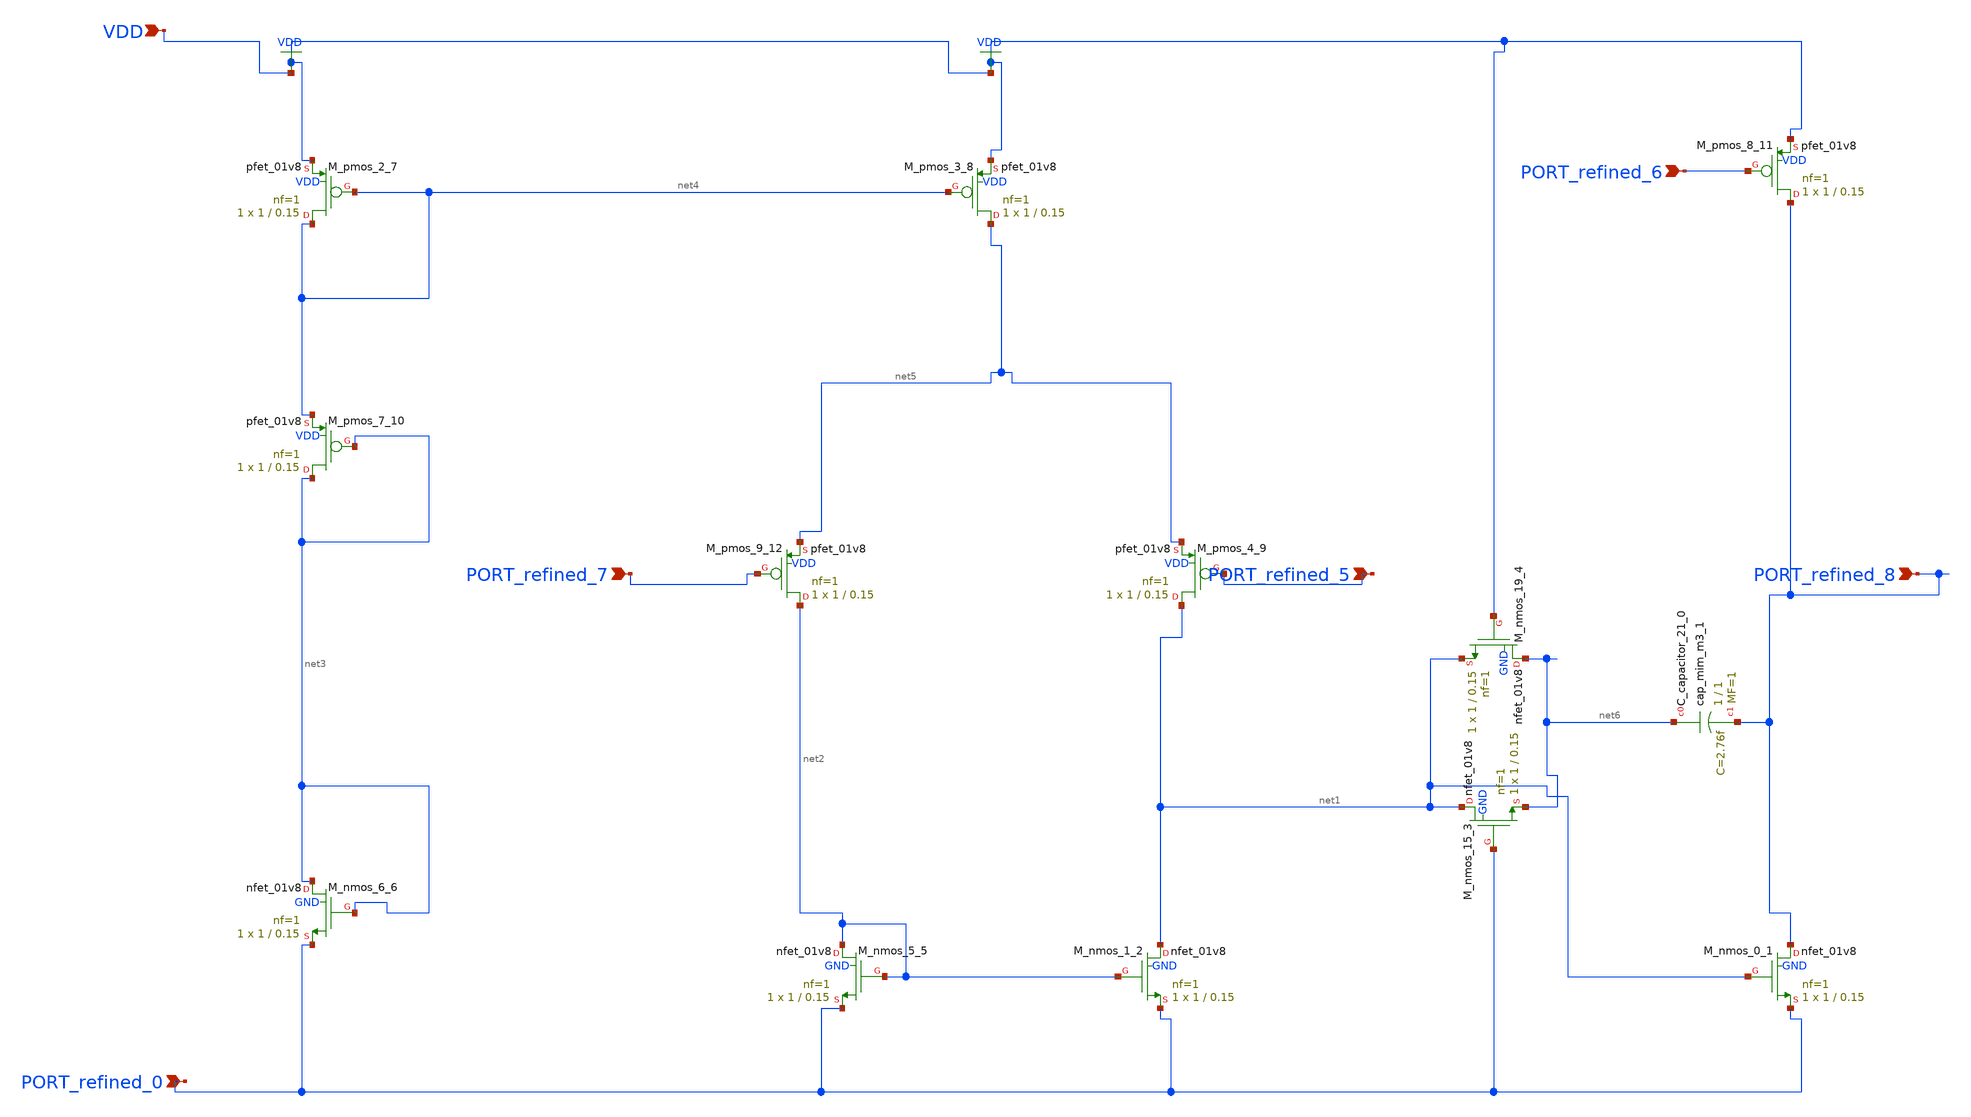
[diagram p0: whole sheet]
** sch_path: schematics/p04_fig4_ota.sch
**.subckt p04_fig4_ota PORT_refined_8 PORT_refined_7 PORT_refined_5 VDD PORT_refined_0
*+ PORT_refined_6
*.ipin PORT_refined_8
*.ipin PORT_refined_7
*.ipin PORT_refined_5
*.ipin VDD
*.ipin PORT_refined_0
*.ipin PORT_refined_6
XC_capacitor_21_0 net6 PORT_refined_8 sky130_fd_pr__cap_mim_m3_1 W=1 L=1 MF=1 m=1
XM_nmos_0_1 PORT_refined_8 net1 PORT_refined_0 GND sky130_fd_pr__nfet_01v8 L=0.15 W=1 nf=1 ad='int((1 + 1)/2) * 1 / 1 * 0.29'
+ as='int((1 + 2)/2) * 1 / 1 * 0.29' pd='2*int((1 + 1)/2) * (1 / 1 + 0.29)' ps='2*int((1 + 2)/2) * (1 / 1 + 0.29)'
+ nrd='0.29 / 1 ' nrs='0.29 / 1 ' sa=0 sb=0 sd=0 mult=1 m=1
XM_nmos_1_2 net1 net2 PORT_refined_0 GND sky130_fd_pr__nfet_01v8 L=0.15 W=1 nf=1 ad='int((1 + 1)/2) * 1 / 1 * 0.29'
+ as='int((1 + 2)/2) * 1 / 1 * 0.29' pd='2*int((1 + 1)/2) * (1 / 1 + 0.29)' ps='2*int((1 + 2)/2) * (1 / 1 + 0.29)'
+ nrd='0.29 / 1 ' nrs='0.29 / 1 ' sa=0 sb=0 sd=0 mult=1 m=1
XM_nmos_15_3 net1 PORT_refined_0 net6 GND sky130_fd_pr__nfet_01v8 L=0.15 W=1 nf=1 ad='int((1 + 1)/2) * 1 / 1 * 0.29'
+ as='int((1 + 2)/2) * 1 / 1 * 0.29' pd='2*int((1 + 1)/2) * (1 / 1 + 0.29)' ps='2*int((1 + 2)/2) * (1 / 1 + 0.29)'
+ nrd='0.29 / 1 ' nrs='0.29 / 1 ' sa=0 sb=0 sd=0 mult=1 m=1
XM_nmos_19_4 net6 VDD net1 GND sky130_fd_pr__nfet_01v8 L=0.15 W=1 nf=1 ad='int((1 + 1)/2) * 1 / 1 * 0.29'
+ as='int((1 + 2)/2) * 1 / 1 * 0.29' pd='2*int((1 + 1)/2) * (1 / 1 + 0.29)' ps='2*int((1 + 2)/2) * (1 / 1 + 0.29)'
+ nrd='0.29 / 1 ' nrs='0.29 / 1 ' sa=0 sb=0 sd=0 mult=1 m=1
XM_nmos_5_5 net2 net2 PORT_refined_0 GND sky130_fd_pr__nfet_01v8 L=0.15 W=1 nf=1 ad='int((1 + 1)/2) * 1 / 1 * 0.29'
+ as='int((1 + 2)/2) * 1 / 1 * 0.29' pd='2*int((1 + 1)/2) * (1 / 1 + 0.29)' ps='2*int((1 + 2)/2) * (1 / 1 + 0.29)'
+ nrd='0.29 / 1 ' nrs='0.29 / 1 ' sa=0 sb=0 sd=0 mult=1 m=1
XM_nmos_6_6 net3 net3 PORT_refined_0 GND sky130_fd_pr__nfet_01v8 L=0.15 W=1 nf=1 ad='int((1 + 1)/2) * 1 / 1 * 0.29'
+ as='int((1 + 2)/2) * 1 / 1 * 0.29' pd='2*int((1 + 1)/2) * (1 / 1 + 0.29)' ps='2*int((1 + 2)/2) * (1 / 1 + 0.29)'
+ nrd='0.29 / 1 ' nrs='0.29 / 1 ' sa=0 sb=0 sd=0 mult=1 m=1
XM_pmos_2_7 net4 net4 VDD VDD sky130_fd_pr__pfet_01v8 L=0.15 W=1 nf=1 ad='int((1 + 1)/2) * 1 / 1 * 0.29'
+ as='int((1 + 2)/2) * 1 / 1 * 0.29' pd='2*int((1 + 1)/2) * (1 / 1 + 0.29)' ps='2*int((1 + 2)/2) * (1 / 1 + 0.29)'
+ nrd='0.29 / 1 ' nrs='0.29 / 1 ' sa=0 sb=0 sd=0 mult=1 m=1
XM_pmos_3_8 net5 net4 VDD VDD sky130_fd_pr__pfet_01v8 L=0.15 W=1 nf=1 ad='int((1 + 1)/2) * 1 / 1 * 0.29'
+ as='int((1 + 2)/2) * 1 / 1 * 0.29' pd='2*int((1 + 1)/2) * (1 / 1 + 0.29)' ps='2*int((1 + 2)/2) * (1 / 1 + 0.29)'
+ nrd='0.29 / 1 ' nrs='0.29 / 1 ' sa=0 sb=0 sd=0 mult=1 m=1
XM_pmos_4_9 net1 PORT_refined_5 net5 VDD sky130_fd_pr__pfet_01v8 L=0.15 W=1 nf=1 ad='int((1 + 1)/2) * 1 / 1 * 0.29'
+ as='int((1 + 2)/2) * 1 / 1 * 0.29' pd='2*int((1 + 1)/2) * (1 / 1 + 0.29)' ps='2*int((1 + 2)/2) * (1 / 1 + 0.29)'
+ nrd='0.29 / 1 ' nrs='0.29 / 1 ' sa=0 sb=0 sd=0 mult=1 m=1
XM_pmos_7_10 net3 net3 net4 VDD sky130_fd_pr__pfet_01v8 L=0.15 W=1 nf=1 ad='int((1 + 1)/2) * 1 / 1 * 0.29'
+ as='int((1 + 2)/2) * 1 / 1 * 0.29' pd='2*int((1 + 1)/2) * (1 / 1 + 0.29)' ps='2*int((1 + 2)/2) * (1 / 1 + 0.29)'
+ nrd='0.29 / 1 ' nrs='0.29 / 1 ' sa=0 sb=0 sd=0 mult=1 m=1
XM_pmos_8_11 PORT_refined_8 PORT_refined_6 VDD VDD sky130_fd_pr__pfet_01v8 L=0.15 W=1 nf=1 ad='int((1 + 1)/2) * 1 / 1 * 0.29'
+ as='int((1 + 2)/2) * 1 / 1 * 0.29' pd='2*int((1 + 1)/2) * (1 / 1 + 0.29)' ps='2*int((1 + 2)/2) * (1 / 1 + 0.29)'
+ nrd='0.29 / 1 ' nrs='0.29 / 1 ' sa=0 sb=0 sd=0 mult=1 m=1
XM_pmos_9_12 net2 PORT_refined_7 net5 VDD sky130_fd_pr__pfet_01v8 L=0.15 W=1 nf=1 ad='int((1 + 1)/2) * 1 / 1 * 0.29'
+ as='int((1 + 2)/2) * 1 / 1 * 0.29' pd='2*int((1 + 1)/2) * (1 / 1 + 0.29)' ps='2*int((1 + 2)/2) * (1 / 1 + 0.29)'
+ nrd='0.29 / 1 ' nrs='0.29 / 1 ' sa=0 sb=0 sd=0 mult=1 m=1
**.ends
.GLOBAL VDD
.end
